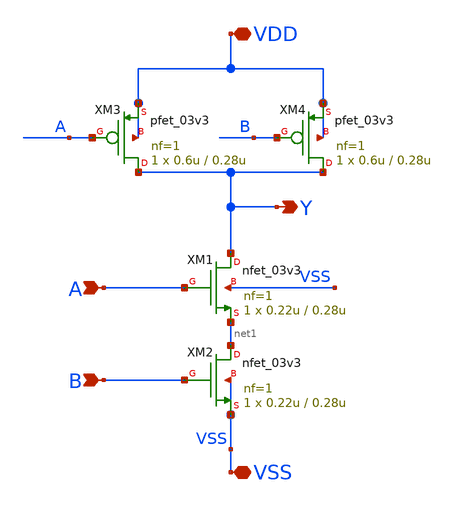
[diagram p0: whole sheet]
** sch_path: src/UN_PFD_GF180mcuD/UN_NAND2_GF180mcuD.sch
**.subckt UN_NAND2_GF180mcuD VDD VSS A B Y
*.iopin VDD
*.iopin VSS
*.ipin A
*.ipin B
*.opin Y
XM1 Y A net1 VSS nfet_03v3 L=0.28u W=0.22u nf=1 ad='int((nf+1)/2) * W/nf * 0.18u' as='int((nf+2)/2) * W/nf * 0.18u'
+ pd='2*int((nf+1)/2) * (W/nf + 0.18u)' ps='2*int((nf+2)/2) * (W/nf + 0.18u)' nrd='0.18u / W' nrs='0.18u / W'
+ sa=0 sb=0 sd=0 m=1
XM2 net1 B VSS VSS nfet_03v3 L=0.28u W=0.22u nf=1 ad='int((nf+1)/2) * W/nf * 0.18u' as='int((nf+2)/2) * W/nf * 0.18u'
+ pd='2*int((nf+1)/2) * (W/nf + 0.18u)' ps='2*int((nf+2)/2) * (W/nf + 0.18u)' nrd='0.18u / W' nrs='0.18u / W'
+ sa=0 sb=0 sd=0 m=1
XM3 Y A VDD VDD pfet_03v3 L=0.28u W=0.6u nf=1 ad='int((nf+1)/2) * W/nf * 0.18u' as='int((nf+2)/2) * W/nf * 0.18u'
+ pd='2*int((nf+1)/2) * (W/nf + 0.18u)' ps='2*int((nf+2)/2) * (W/nf + 0.18u)' nrd='0.18u / W' nrs='0.18u / W'
+ sa=0 sb=0 sd=0 m=1
XM4 Y B VDD VDD pfet_03v3 L=0.28u W=0.6u nf=1 ad='int((nf+1)/2) * W/nf * 0.18u' as='int((nf+2)/2) * W/nf * 0.18u'
+ pd='2*int((nf+1)/2) * (W/nf + 0.18u)' ps='2*int((nf+2)/2) * (W/nf + 0.18u)' nrd='0.18u / W' nrs='0.18u / W'
+ sa=0 sb=0 sd=0 m=1
**.ends
.end
